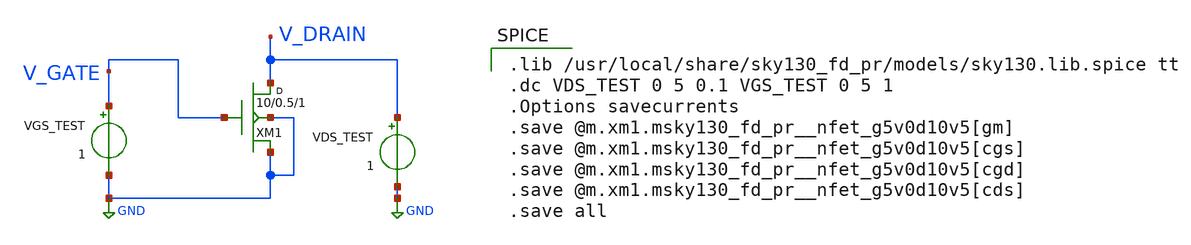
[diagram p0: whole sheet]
** sch_path: device/sims/fet_sweep.sch
**.subckt fet_sweep
VGS_TEST V_GATE GND 1
XM1 V_DRAIN V_GATE GND GND sky130_fd_pr__nfet_g5v0d10v5 w=10 l=0.5 m=1
VDS_TEST V_DRAIN GND 1
**** begin user architecture code

.lib /usr/local/share/sky130_fd_pr/models/sky130.lib.spice tt
.dc VDS_TEST 0 5 0.1 VGS_TEST 0 5 1
.Options savecurrents
.save @m.xm1.msky130_fd_pr__nfet_g5v0d10v5[gm]
.save @m.xm1.msky130_fd_pr__nfet_g5v0d10v5[cgs]
.save @m.xm1.msky130_fd_pr__nfet_g5v0d10v5[cgd]
.save @m.xm1.msky130_fd_pr__nfet_g5v0d10v5[cds]
.save all

**** end user architecture code
**.ends
.GLOBAL GND
.end
